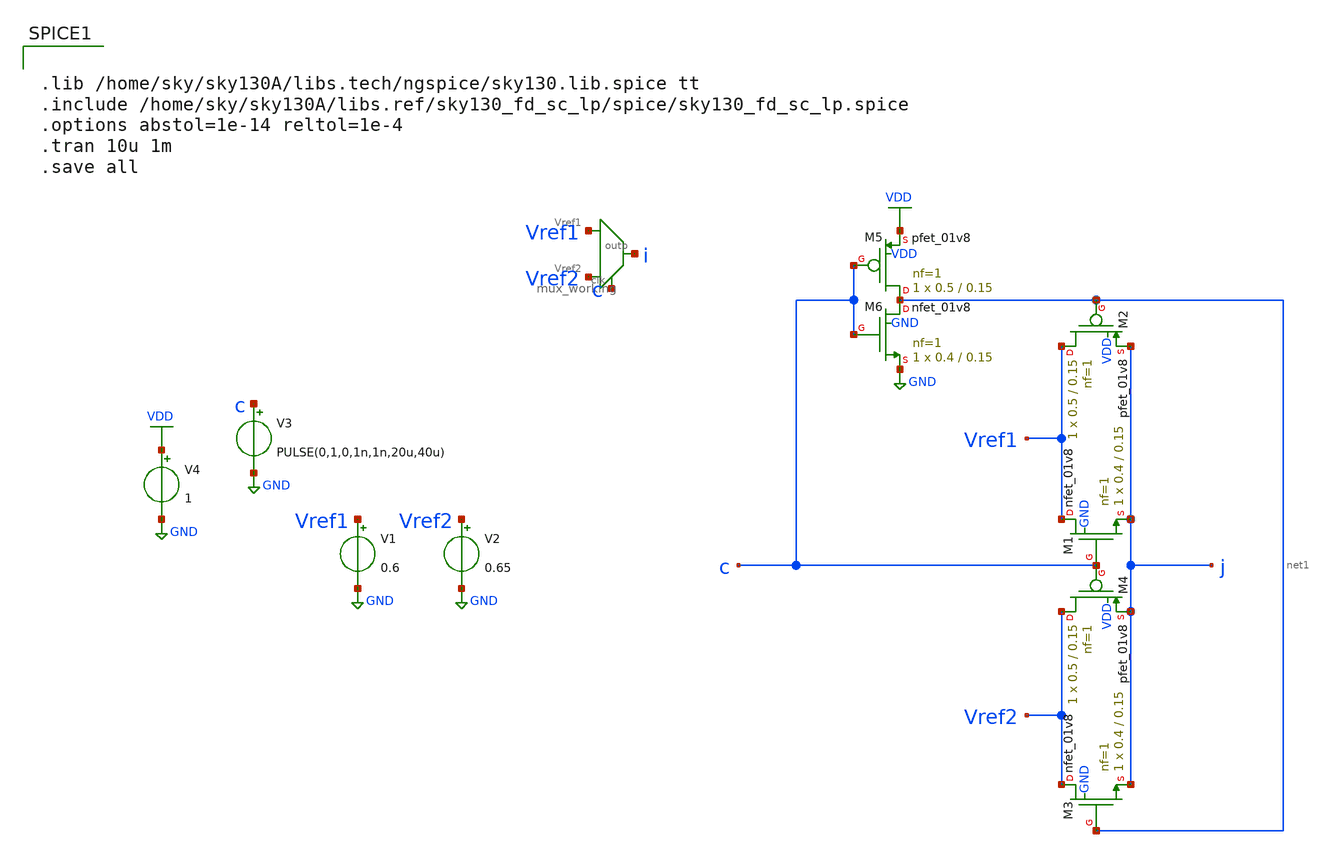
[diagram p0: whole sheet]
** sch_path: xschem/comparator/mux_tb.sch
**.subckt mux_tb
V1 Vref1 GND 0.6
V2 Vref2 GND 0.65
V3 c GND PULSE(0,1,0,1n,1n,20u,40u)
V4 VDD GND 1
XM1 Vref1 c j GND sky130_fd_pr__nfet_01v8 L=0.15 W=0.4 nf=1 ad='int((nf+1)/2) * W/nf * 0.29' as='int((nf+2)/2) * W/nf * 0.29'
+ pd='2*int((nf+1)/2) * (W/nf + 0.29)' ps='2*int((nf+2)/2) * (W/nf + 0.29)' nrd='0.29 / W' nrs='0.29 / W'
+ sa=0 sb=0 sd=0 mult=1 m=1
XM2 Vref1 net1 j VDD sky130_fd_pr__pfet_01v8 L=0.15 W=0.5 nf=1 ad='int((nf+1)/2) * W/nf * 0.29' as='int((nf+2)/2) * W/nf * 0.29'
+ pd='2*int((nf+1)/2) * (W/nf + 0.29)' ps='2*int((nf+2)/2) * (W/nf + 0.29)' nrd='0.29 / W' nrs='0.29 / W'
+ sa=0 sb=0 sd=0 mult=1 m=1
XM3 Vref2 net1 j GND sky130_fd_pr__nfet_01v8 L=0.15 W=0.4 nf=1 ad='int((nf+1)/2) * W/nf * 0.29' as='int((nf+2)/2) * W/nf * 0.29'
+ pd='2*int((nf+1)/2) * (W/nf + 0.29)' ps='2*int((nf+2)/2) * (W/nf + 0.29)' nrd='0.29 / W' nrs='0.29 / W'
+ sa=0 sb=0 sd=0 mult=1 m=1
XM4 Vref2 c j VDD sky130_fd_pr__pfet_01v8 L=0.15 W=0.5 nf=1 ad='int((nf+1)/2) * W/nf * 0.29' as='int((nf+2)/2) * W/nf * 0.29'
+ pd='2*int((nf+1)/2) * (W/nf + 0.29)' ps='2*int((nf+2)/2) * (W/nf + 0.29)' nrd='0.29 / W' nrs='0.29 / W'
+ sa=0 sb=0 sd=0 mult=1 m=1
XM5 net1 c VDD VDD sky130_fd_pr__pfet_01v8 L=0.15 W=0.5 nf=1 ad='int((nf+1)/2) * W/nf * 0.29' as='int((nf+2)/2) * W/nf * 0.29'
+ pd='2*int((nf+1)/2) * (W/nf + 0.29)' ps='2*int((nf+2)/2) * (W/nf + 0.29)' nrd='0.29 / W' nrs='0.29 / W'
+ sa=0 sb=0 sd=0 mult=1 m=1
XM6 net1 c GND GND sky130_fd_pr__nfet_01v8 L=0.15 W=0.4 nf=1 ad='int((nf+1)/2) * W/nf * 0.29' as='int((nf+2)/2) * W/nf * 0.29'
+ pd='2*int((nf+1)/2) * (W/nf + 0.29)' ps='2*int((nf+2)/2) * (W/nf + 0.29)' nrd='0.29 / W' nrs='0.29 / W'
+ sa=0 sb=0 sd=0 mult=1 m=1
X1 Vref1 Vref2 i c mux_working
**** begin user architecture code


.lib /home/sky/sky130A/libs.tech/ngspice/sky130.lib.spice tt
.include /home/sky/sky130A/libs.ref/sky130_fd_sc_lp/spice/sky130_fd_sc_lp.spice
.options abstol=1e-14 reltol=1e-4
.tran 10u 1m
.save all


**** end user architecture code
**.ends

* expanding   symbol:  /home/sky/fossi_cochlea/xschem/comparator/mux_working.sym # of pins=4
** sym_path: xschem/comparator/mux_working.sym
** sch_path: xschem/comparator/mux_working.sch
.subckt mux_working Vref1 Vref2 outp clk
*.ipin Vref2
*.opin outp
*.ipin clk
*.ipin Vref1
XM1 Vref1 clk outp GND sky130_fd_pr__nfet_01v8 L=0.15 W=0.4 nf=1 ad='int((nf+1)/2) * W/nf * 0.29' as='int((nf+2)/2) * W/nf * 0.29'
+ pd='2*int((nf+1)/2) * (W/nf + 0.29)' ps='2*int((nf+2)/2) * (W/nf + 0.29)' nrd='0.29 / W' nrs='0.29 / W'
+ sa=0 sb=0 sd=0 mult=1 m=1
XM2 Vref1 net1 outp VDD sky130_fd_pr__pfet_01v8 L=0.15 W=1 nf=1 ad='int((nf+1)/2) * W/nf * 0.29' as='int((nf+2)/2) * W/nf * 0.29'
+ pd='2*int((nf+1)/2) * (W/nf + 0.29)' ps='2*int((nf+2)/2) * (W/nf + 0.29)' nrd='0.29 / W' nrs='0.29 / W'
+ sa=0 sb=0 sd=0 mult=1 m=1
XM3 Vref2 net1 outp GND sky130_fd_pr__nfet_01v8 L=0.15 W=0.4 nf=1 ad='int((nf+1)/2) * W/nf * 0.29' as='int((nf+2)/2) * W/nf * 0.29'
+ pd='2*int((nf+1)/2) * (W/nf + 0.29)' ps='2*int((nf+2)/2) * (W/nf + 0.29)' nrd='0.29 / W' nrs='0.29 / W'
+ sa=0 sb=0 sd=0 mult=1 m=1
XM4 Vref2 clk outp VDD sky130_fd_pr__pfet_01v8 L=0.15 W=1 nf=1 ad='int((nf+1)/2) * W/nf * 0.29' as='int((nf+2)/2) * W/nf * 0.29'
+ pd='2*int((nf+1)/2) * (W/nf + 0.29)' ps='2*int((nf+2)/2) * (W/nf + 0.29)' nrd='0.29 / W' nrs='0.29 / W'
+ sa=0 sb=0 sd=0 mult=1 m=1
XM5 net1 clk VDD VDD sky130_fd_pr__pfet_01v8 L=0.15 W=1 nf=1 ad='int((nf+1)/2) * W/nf * 0.29' as='int((nf+2)/2) * W/nf * 0.29'
+ pd='2*int((nf+1)/2) * (W/nf + 0.29)' ps='2*int((nf+2)/2) * (W/nf + 0.29)' nrd='0.29 / W' nrs='0.29 / W'
+ sa=0 sb=0 sd=0 mult=1 m=1
XM6 net1 clk GND GND sky130_fd_pr__nfet_01v8 L=0.15 W=0.4 nf=1 ad='int((nf+1)/2) * W/nf * 0.29' as='int((nf+2)/2) * W/nf * 0.29'
+ pd='2*int((nf+1)/2) * (W/nf + 0.29)' ps='2*int((nf+2)/2) * (W/nf + 0.29)' nrd='0.29 / W' nrs='0.29 / W'
+ sa=0 sb=0 sd=0 mult=1 m=1
.ends

.GLOBAL GND
.GLOBAL VDD
.end
